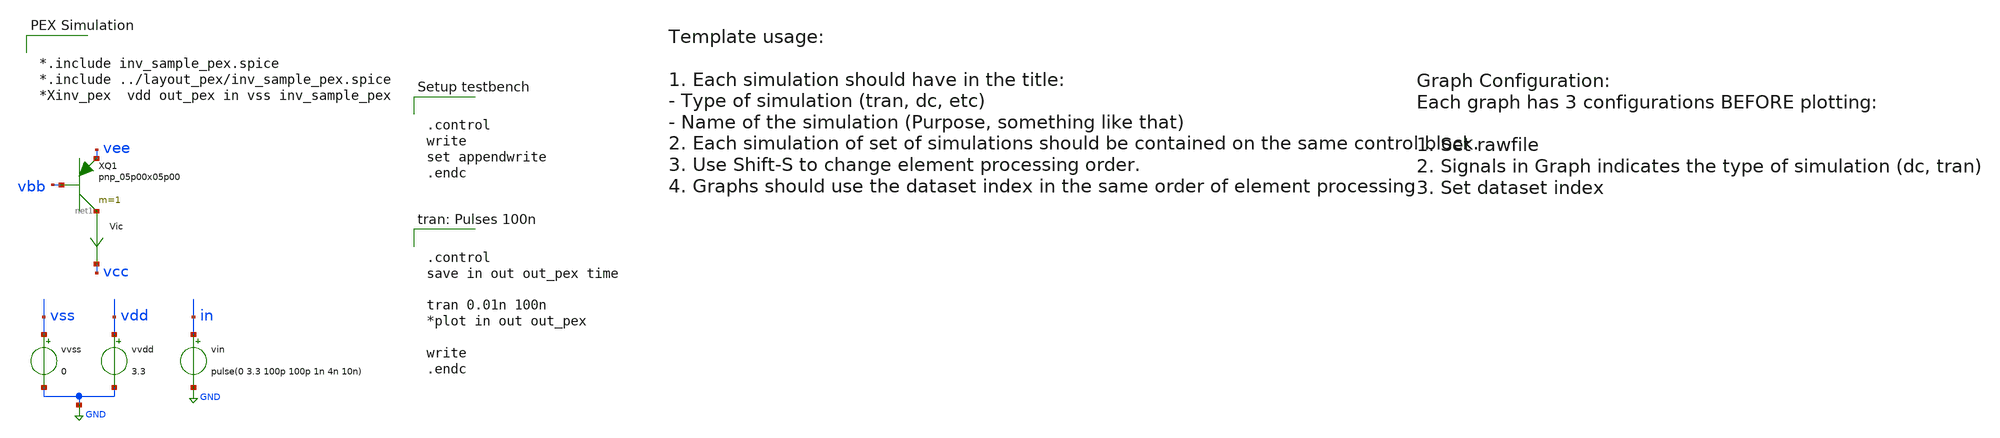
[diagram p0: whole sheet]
** sch_path: samples/gf180mcu/bjt_fast/test/bjt_test.sch

.include $env(PDK_ROOT)/$env(PDK)/libs.tech/ngspice/design.ngspice
.lib $env(PDK_ROOT)/$env(PDK)/libs.tech/ngspice/sm141064.ngspice typical
.lib $env(PDK_ROOT)/$env(PDK)/libs.tech/ngspice/sm141064.ngspice mimcap_statistical
.lib $env(PDK_ROOT)/$env(PDK)/libs.tech/ngspice/sm141064.ngspice cap_mim
.lib $env(PDK_ROOT)/$env(PDK)/libs.tech/ngspice/sm141064.ngspice res_typical
.lib $env(PDK_ROOT)/$env(PDK)/libs.tech/ngspice/sm141064.ngspice bjt_typical
.lib $env(PDK_ROOT)/$env(PDK)/libs.tech/ngspice/sm141064.ngspice moscap_typical


.control
write
set appendwrite
.endc


**.subckt bjt_test
vvdd vdd GND 3.3
vin in GND pulse(0 3.3 100p 100p 1n 4n 10n)
vvss vss GND 0
XQ1 net1 vbb vee pnp_05p00x05p00 m=1 par=1
Vic net1 vcc 0
.save i(vic)
**** begin user architecture code


.control
save in out out_pex time

tran 0.01n 100n
*plot in out out_pex

write
.endc




*.include inv_sample_pex.spice
*.include ../layout_pex/inv_sample_pex.spice
*Xinv_pex  vdd out_pex in vss inv_sample_pex


**** end user architecture code
**.ends
.GLOBAL GND
.end
